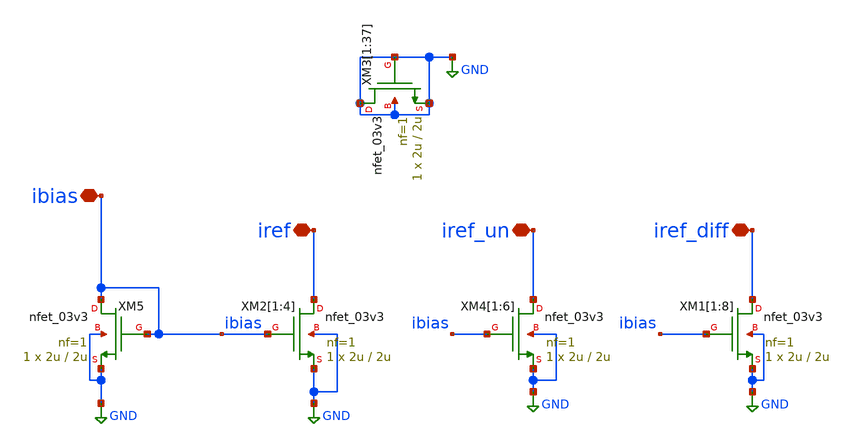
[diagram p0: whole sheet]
** sch_path: Voltage_Reference/LDO/CM_block.sch
**.subckt CM_block ibias iref iref_un iref_diff
*.iopin ibias
*.iopin iref
*.iopin iref_un
*.iopin iref_diff
XM4[1] iref_un ibias GND GND nfet_03v3 L=2u W=2u nf=1 ad='int((nf+1)/2) * W/nf * 0.18u' as='int((nf+2)/2) * W/nf * 0.18u'
+ pd='2*int((nf+1)/2) * (W/nf + 0.18u)' ps='2*int((nf+2)/2) * (W/nf + 0.18u)' nrd='0.18u / W' nrs='0.18u / W'
+ sa=0 sb=0 sd=0 m=1
XM4[2] iref_un ibias GND GND nfet_03v3 L=2u W=2u nf=1 ad='int((nf+1)/2) * W/nf * 0.18u' as='int((nf+2)/2) * W/nf * 0.18u'
+ pd='2*int((nf+1)/2) * (W/nf + 0.18u)' ps='2*int((nf+2)/2) * (W/nf + 0.18u)' nrd='0.18u / W' nrs='0.18u / W'
+ sa=0 sb=0 sd=0 m=1
XM4[3] iref_un ibias GND GND nfet_03v3 L=2u W=2u nf=1 ad='int((nf+1)/2) * W/nf * 0.18u' as='int((nf+2)/2) * W/nf * 0.18u'
+ pd='2*int((nf+1)/2) * (W/nf + 0.18u)' ps='2*int((nf+2)/2) * (W/nf + 0.18u)' nrd='0.18u / W' nrs='0.18u / W'
+ sa=0 sb=0 sd=0 m=1
XM4[4] iref_un ibias GND GND nfet_03v3 L=2u W=2u nf=1 ad='int((nf+1)/2) * W/nf * 0.18u' as='int((nf+2)/2) * W/nf * 0.18u'
+ pd='2*int((nf+1)/2) * (W/nf + 0.18u)' ps='2*int((nf+2)/2) * (W/nf + 0.18u)' nrd='0.18u / W' nrs='0.18u / W'
+ sa=0 sb=0 sd=0 m=1
XM4[5] iref_un ibias GND GND nfet_03v3 L=2u W=2u nf=1 ad='int((nf+1)/2) * W/nf * 0.18u' as='int((nf+2)/2) * W/nf * 0.18u'
+ pd='2*int((nf+1)/2) * (W/nf + 0.18u)' ps='2*int((nf+2)/2) * (W/nf + 0.18u)' nrd='0.18u / W' nrs='0.18u / W'
+ sa=0 sb=0 sd=0 m=1
XM4[6] iref_un ibias GND GND nfet_03v3 L=2u W=2u nf=1 ad='int((nf+1)/2) * W/nf * 0.18u' as='int((nf+2)/2) * W/nf * 0.18u'
+ pd='2*int((nf+1)/2) * (W/nf + 0.18u)' ps='2*int((nf+2)/2) * (W/nf + 0.18u)' nrd='0.18u / W' nrs='0.18u / W'
+ sa=0 sb=0 sd=0 m=1
XM1[1] iref_diff ibias GND GND nfet_03v3 L=2u W=2u nf=1 ad='int((nf+1)/2) * W/nf * 0.18u' as='int((nf+2)/2) * W/nf * 0.18u'
+ pd='2*int((nf+1)/2) * (W/nf + 0.18u)' ps='2*int((nf+2)/2) * (W/nf + 0.18u)' nrd='0.18u / W' nrs='0.18u / W'
+ sa=0 sb=0 sd=0 m=1
XM1[2] iref_diff ibias GND GND nfet_03v3 L=2u W=2u nf=1 ad='int((nf+1)/2) * W/nf * 0.18u' as='int((nf+2)/2) * W/nf * 0.18u'
+ pd='2*int((nf+1)/2) * (W/nf + 0.18u)' ps='2*int((nf+2)/2) * (W/nf + 0.18u)' nrd='0.18u / W' nrs='0.18u / W'
+ sa=0 sb=0 sd=0 m=1
XM1[3] iref_diff ibias GND GND nfet_03v3 L=2u W=2u nf=1 ad='int((nf+1)/2) * W/nf * 0.18u' as='int((nf+2)/2) * W/nf * 0.18u'
+ pd='2*int((nf+1)/2) * (W/nf + 0.18u)' ps='2*int((nf+2)/2) * (W/nf + 0.18u)' nrd='0.18u / W' nrs='0.18u / W'
+ sa=0 sb=0 sd=0 m=1
XM1[4] iref_diff ibias GND GND nfet_03v3 L=2u W=2u nf=1 ad='int((nf+1)/2) * W/nf * 0.18u' as='int((nf+2)/2) * W/nf * 0.18u'
+ pd='2*int((nf+1)/2) * (W/nf + 0.18u)' ps='2*int((nf+2)/2) * (W/nf + 0.18u)' nrd='0.18u / W' nrs='0.18u / W'
+ sa=0 sb=0 sd=0 m=1
XM1[5] iref_diff ibias GND GND nfet_03v3 L=2u W=2u nf=1 ad='int((nf+1)/2) * W/nf * 0.18u' as='int((nf+2)/2) * W/nf * 0.18u'
+ pd='2*int((nf+1)/2) * (W/nf + 0.18u)' ps='2*int((nf+2)/2) * (W/nf + 0.18u)' nrd='0.18u / W' nrs='0.18u / W'
+ sa=0 sb=0 sd=0 m=1
XM1[6] iref_diff ibias GND GND nfet_03v3 L=2u W=2u nf=1 ad='int((nf+1)/2) * W/nf * 0.18u' as='int((nf+2)/2) * W/nf * 0.18u'
+ pd='2*int((nf+1)/2) * (W/nf + 0.18u)' ps='2*int((nf+2)/2) * (W/nf + 0.18u)' nrd='0.18u / W' nrs='0.18u / W'
+ sa=0 sb=0 sd=0 m=1
XM1[7] iref_diff ibias GND GND nfet_03v3 L=2u W=2u nf=1 ad='int((nf+1)/2) * W/nf * 0.18u' as='int((nf+2)/2) * W/nf * 0.18u'
+ pd='2*int((nf+1)/2) * (W/nf + 0.18u)' ps='2*int((nf+2)/2) * (W/nf + 0.18u)' nrd='0.18u / W' nrs='0.18u / W'
+ sa=0 sb=0 sd=0 m=1
XM1[8] iref_diff ibias GND GND nfet_03v3 L=2u W=2u nf=1 ad='int((nf+1)/2) * W/nf * 0.18u' as='int((nf+2)/2) * W/nf * 0.18u'
+ pd='2*int((nf+1)/2) * (W/nf + 0.18u)' ps='2*int((nf+2)/2) * (W/nf + 0.18u)' nrd='0.18u / W' nrs='0.18u / W'
+ sa=0 sb=0 sd=0 m=1
XM2[1] iref ibias GND GND nfet_03v3 L=2u W=2u nf=1 ad='int((nf+1)/2) * W/nf * 0.18u' as='int((nf+2)/2) * W/nf * 0.18u'
+ pd='2*int((nf+1)/2) * (W/nf + 0.18u)' ps='2*int((nf+2)/2) * (W/nf + 0.18u)' nrd='0.18u / W' nrs='0.18u / W'
+ sa=0 sb=0 sd=0 m=1
XM2[2] iref ibias GND GND nfet_03v3 L=2u W=2u nf=1 ad='int((nf+1)/2) * W/nf * 0.18u' as='int((nf+2)/2) * W/nf * 0.18u'
+ pd='2*int((nf+1)/2) * (W/nf + 0.18u)' ps='2*int((nf+2)/2) * (W/nf + 0.18u)' nrd='0.18u / W' nrs='0.18u / W'
+ sa=0 sb=0 sd=0 m=1
XM2[3] iref ibias GND GND nfet_03v3 L=2u W=2u nf=1 ad='int((nf+1)/2) * W/nf * 0.18u' as='int((nf+2)/2) * W/nf * 0.18u'
+ pd='2*int((nf+1)/2) * (W/nf + 0.18u)' ps='2*int((nf+2)/2) * (W/nf + 0.18u)' nrd='0.18u / W' nrs='0.18u / W'
+ sa=0 sb=0 sd=0 m=1
XM2[4] iref ibias GND GND nfet_03v3 L=2u W=2u nf=1 ad='int((nf+1)/2) * W/nf * 0.18u' as='int((nf+2)/2) * W/nf * 0.18u'
+ pd='2*int((nf+1)/2) * (W/nf + 0.18u)' ps='2*int((nf+2)/2) * (W/nf + 0.18u)' nrd='0.18u / W' nrs='0.18u / W'
+ sa=0 sb=0 sd=0 m=1
XM5 ibias ibias GND GND nfet_03v3 L=2u W=2u nf=1 ad='int((nf+1)/2) * W/nf * 0.18u' as='int((nf+2)/2) * W/nf * 0.18u'
+ pd='2*int((nf+1)/2) * (W/nf + 0.18u)' ps='2*int((nf+2)/2) * (W/nf + 0.18u)' nrd='0.18u / W' nrs='0.18u / W'
+ sa=0 sb=0 sd=0 m=1
XM3[1] GND GND GND GND nfet_03v3 L=2u W=2u nf=1 ad='int((nf+1)/2) * W/nf * 0.18u' as='int((nf+2)/2) * W/nf * 0.18u'
+ pd='2*int((nf+1)/2) * (W/nf + 0.18u)' ps='2*int((nf+2)/2) * (W/nf + 0.18u)' nrd='0.18u / W' nrs='0.18u / W'
+ sa=0 sb=0 sd=0 m=1
XM3[2] GND GND GND GND nfet_03v3 L=2u W=2u nf=1 ad='int((nf+1)/2) * W/nf * 0.18u' as='int((nf+2)/2) * W/nf * 0.18u'
+ pd='2*int((nf+1)/2) * (W/nf + 0.18u)' ps='2*int((nf+2)/2) * (W/nf + 0.18u)' nrd='0.18u / W' nrs='0.18u / W'
+ sa=0 sb=0 sd=0 m=1
XM3[3] GND GND GND GND nfet_03v3 L=2u W=2u nf=1 ad='int((nf+1)/2) * W/nf * 0.18u' as='int((nf+2)/2) * W/nf * 0.18u'
+ pd='2*int((nf+1)/2) * (W/nf + 0.18u)' ps='2*int((nf+2)/2) * (W/nf + 0.18u)' nrd='0.18u / W' nrs='0.18u / W'
+ sa=0 sb=0 sd=0 m=1
XM3[4] GND GND GND GND nfet_03v3 L=2u W=2u nf=1 ad='int((nf+1)/2) * W/nf * 0.18u' as='int((nf+2)/2) * W/nf * 0.18u'
+ pd='2*int((nf+1)/2) * (W/nf + 0.18u)' ps='2*int((nf+2)/2) * (W/nf + 0.18u)' nrd='0.18u / W' nrs='0.18u / W'
+ sa=0 sb=0 sd=0 m=1
XM3[5] GND GND GND GND nfet_03v3 L=2u W=2u nf=1 ad='int((nf+1)/2) * W/nf * 0.18u' as='int((nf+2)/2) * W/nf * 0.18u'
+ pd='2*int((nf+1)/2) * (W/nf + 0.18u)' ps='2*int((nf+2)/2) * (W/nf + 0.18u)' nrd='0.18u / W' nrs='0.18u / W'
+ sa=0 sb=0 sd=0 m=1
XM3[6] GND GND GND GND nfet_03v3 L=2u W=2u nf=1 ad='int((nf+1)/2) * W/nf * 0.18u' as='int((nf+2)/2) * W/nf * 0.18u'
+ pd='2*int((nf+1)/2) * (W/nf + 0.18u)' ps='2*int((nf+2)/2) * (W/nf + 0.18u)' nrd='0.18u / W' nrs='0.18u / W'
+ sa=0 sb=0 sd=0 m=1
XM3[7] GND GND GND GND nfet_03v3 L=2u W=2u nf=1 ad='int((nf+1)/2) * W/nf * 0.18u' as='int((nf+2)/2) * W/nf * 0.18u'
+ pd='2*int((nf+1)/2) * (W/nf + 0.18u)' ps='2*int((nf+2)/2) * (W/nf + 0.18u)' nrd='0.18u / W' nrs='0.18u / W'
+ sa=0 sb=0 sd=0 m=1
XM3[8] GND GND GND GND nfet_03v3 L=2u W=2u nf=1 ad='int((nf+1)/2) * W/nf * 0.18u' as='int((nf+2)/2) * W/nf * 0.18u'
+ pd='2*int((nf+1)/2) * (W/nf + 0.18u)' ps='2*int((nf+2)/2) * (W/nf + 0.18u)' nrd='0.18u / W' nrs='0.18u / W'
+ sa=0 sb=0 sd=0 m=1
XM3[9] GND GND GND GND nfet_03v3 L=2u W=2u nf=1 ad='int((nf+1)/2) * W/nf * 0.18u' as='int((nf+2)/2) * W/nf * 0.18u'
+ pd='2*int((nf+1)/2) * (W/nf + 0.18u)' ps='2*int((nf+2)/2) * (W/nf + 0.18u)' nrd='0.18u / W' nrs='0.18u / W'
+ sa=0 sb=0 sd=0 m=1
XM3[10] GND GND GND GND nfet_03v3 L=2u W=2u nf=1 ad='int((nf+1)/2) * W/nf * 0.18u' as='int((nf+2)/2) * W/nf * 0.18u'
+ pd='2*int((nf+1)/2) * (W/nf + 0.18u)' ps='2*int((nf+2)/2) * (W/nf + 0.18u)' nrd='0.18u / W' nrs='0.18u / W'
+ sa=0 sb=0 sd=0 m=1
XM3[11] GND GND GND GND nfet_03v3 L=2u W=2u nf=1 ad='int((nf+1)/2) * W/nf * 0.18u' as='int((nf+2)/2) * W/nf * 0.18u'
+ pd='2*int((nf+1)/2) * (W/nf + 0.18u)' ps='2*int((nf+2)/2) * (W/nf + 0.18u)' nrd='0.18u / W' nrs='0.18u / W'
+ sa=0 sb=0 sd=0 m=1
XM3[12] GND GND GND GND nfet_03v3 L=2u W=2u nf=1 ad='int((nf+1)/2) * W/nf * 0.18u' as='int((nf+2)/2) * W/nf * 0.18u'
+ pd='2*int((nf+1)/2) * (W/nf + 0.18u)' ps='2*int((nf+2)/2) * (W/nf + 0.18u)' nrd='0.18u / W' nrs='0.18u / W'
+ sa=0 sb=0 sd=0 m=1
XM3[13] GND GND GND GND nfet_03v3 L=2u W=2u nf=1 ad='int((nf+1)/2) * W/nf * 0.18u' as='int((nf+2)/2) * W/nf * 0.18u'
+ pd='2*int((nf+1)/2) * (W/nf + 0.18u)' ps='2*int((nf+2)/2) * (W/nf + 0.18u)' nrd='0.18u / W' nrs='0.18u / W'
+ sa=0 sb=0 sd=0 m=1
XM3[14] GND GND GND GND nfet_03v3 L=2u W=2u nf=1 ad='int((nf+1)/2) * W/nf * 0.18u' as='int((nf+2)/2) * W/nf * 0.18u'
+ pd='2*int((nf+1)/2) * (W/nf + 0.18u)' ps='2*int((nf+2)/2) * (W/nf + 0.18u)' nrd='0.18u / W' nrs='0.18u / W'
+ sa=0 sb=0 sd=0 m=1
XM3[15] GND GND GND GND nfet_03v3 L=2u W=2u nf=1 ad='int((nf+1)/2) * W/nf * 0.18u' as='int((nf+2)/2) * W/nf * 0.18u'
+ pd='2*int((nf+1)/2) * (W/nf + 0.18u)' ps='2*int((nf+2)/2) * (W/nf + 0.18u)' nrd='0.18u / W' nrs='0.18u / W'
+ sa=0 sb=0 sd=0 m=1
XM3[16] GND GND GND GND nfet_03v3 L=2u W=2u nf=1 ad='int((nf+1)/2) * W/nf * 0.18u' as='int((nf+2)/2) * W/nf * 0.18u'
+ pd='2*int((nf+1)/2) * (W/nf + 0.18u)' ps='2*int((nf+2)/2) * (W/nf + 0.18u)' nrd='0.18u / W' nrs='0.18u / W'
+ sa=0 sb=0 sd=0 m=1
XM3[17] GND GND GND GND nfet_03v3 L=2u W=2u nf=1 ad='int((nf+1)/2) * W/nf * 0.18u' as='int((nf+2)/2) * W/nf * 0.18u'
+ pd='2*int((nf+1)/2) * (W/nf + 0.18u)' ps='2*int((nf+2)/2) * (W/nf + 0.18u)' nrd='0.18u / W' nrs='0.18u / W'
+ sa=0 sb=0 sd=0 m=1
XM3[18] GND GND GND GND nfet_03v3 L=2u W=2u nf=1 ad='int((nf+1)/2) * W/nf * 0.18u' as='int((nf+2)/2) * W/nf * 0.18u'
+ pd='2*int((nf+1)/2) * (W/nf + 0.18u)' ps='2*int((nf+2)/2) * (W/nf + 0.18u)' nrd='0.18u / W' nrs='0.18u / W'
+ sa=0 sb=0 sd=0 m=1
XM3[19] GND GND GND GND nfet_03v3 L=2u W=2u nf=1 ad='int((nf+1)/2) * W/nf * 0.18u' as='int((nf+2)/2) * W/nf * 0.18u'
+ pd='2*int((nf+1)/2) * (W/nf + 0.18u)' ps='2*int((nf+2)/2) * (W/nf + 0.18u)' nrd='0.18u / W' nrs='0.18u / W'
+ sa=0 sb=0 sd=0 m=1
XM3[20] GND GND GND GND nfet_03v3 L=2u W=2u nf=1 ad='int((nf+1)/2) * W/nf * 0.18u' as='int((nf+2)/2) * W/nf * 0.18u'
+ pd='2*int((nf+1)/2) * (W/nf + 0.18u)' ps='2*int((nf+2)/2) * (W/nf + 0.18u)' nrd='0.18u / W' nrs='0.18u / W'
+ sa=0 sb=0 sd=0 m=1
XM3[21] GND GND GND GND nfet_03v3 L=2u W=2u nf=1 ad='int((nf+1)/2) * W/nf * 0.18u' as='int((nf+2)/2) * W/nf * 0.18u'
+ pd='2*int((nf+1)/2) * (W/nf + 0.18u)' ps='2*int((nf+2)/2) * (W/nf + 0.18u)' nrd='0.18u / W' nrs='0.18u / W'
+ sa=0 sb=0 sd=0 m=1
XM3[22] GND GND GND GND nfet_03v3 L=2u W=2u nf=1 ad='int((nf+1)/2) * W/nf * 0.18u' as='int((nf+2)/2) * W/nf * 0.18u'
+ pd='2*int((nf+1)/2) * (W/nf + 0.18u)' ps='2*int((nf+2)/2) * (W/nf + 0.18u)' nrd='0.18u / W' nrs='0.18u / W'
+ sa=0 sb=0 sd=0 m=1
XM3[23] GND GND GND GND nfet_03v3 L=2u W=2u nf=1 ad='int((nf+1)/2) * W/nf * 0.18u' as='int((nf+2)/2) * W/nf * 0.18u'
+ pd='2*int((nf+1)/2) * (W/nf + 0.18u)' ps='2*int((nf+2)/2) * (W/nf + 0.18u)' nrd='0.18u / W' nrs='0.18u / W'
+ sa=0 sb=0 sd=0 m=1
XM3[24] GND GND GND GND nfet_03v3 L=2u W=2u nf=1 ad='int((nf+1)/2) * W/nf * 0.18u' as='int((nf+2)/2) * W/nf * 0.18u'
+ pd='2*int((nf+1)/2) * (W/nf + 0.18u)' ps='2*int((nf+2)/2) * (W/nf + 0.18u)' nrd='0.18u / W' nrs='0.18u / W'
+ sa=0 sb=0 sd=0 m=1
XM3[25] GND GND GND GND nfet_03v3 L=2u W=2u nf=1 ad='int((nf+1)/2) * W/nf * 0.18u' as='int((nf+2)/2) * W/nf * 0.18u'
+ pd='2*int((nf+1)/2) * (W/nf + 0.18u)' ps='2*int((nf+2)/2) * (W/nf + 0.18u)' nrd='0.18u / W' nrs='0.18u / W'
+ sa=0 sb=0 sd=0 m=1
XM3[26] GND GND GND GND nfet_03v3 L=2u W=2u nf=1 ad='int((nf+1)/2) * W/nf * 0.18u' as='int((nf+2)/2) * W/nf * 0.18u'
+ pd='2*int((nf+1)/2) * (W/nf + 0.18u)' ps='2*int((nf+2)/2) * (W/nf + 0.18u)' nrd='0.18u / W' nrs='0.18u / W'
+ sa=0 sb=0 sd=0 m=1
XM3[27] GND GND GND GND nfet_03v3 L=2u W=2u nf=1 ad='int((nf+1)/2) * W/nf * 0.18u' as='int((nf+2)/2) * W/nf * 0.18u'
+ pd='2*int((nf+1)/2) * (W/nf + 0.18u)' ps='2*int((nf+2)/2) * (W/nf + 0.18u)' nrd='0.18u / W' nrs='0.18u / W'
+ sa=0 sb=0 sd=0 m=1
XM3[28] GND GND GND GND nfet_03v3 L=2u W=2u nf=1 ad='int((nf+1)/2) * W/nf * 0.18u' as='int((nf+2)/2) * W/nf * 0.18u'
+ pd='2*int((nf+1)/2) * (W/nf + 0.18u)' ps='2*int((nf+2)/2) * (W/nf + 0.18u)' nrd='0.18u / W' nrs='0.18u / W'
+ sa=0 sb=0 sd=0 m=1
XM3[29] GND GND GND GND nfet_03v3 L=2u W=2u nf=1 ad='int((nf+1)/2) * W/nf * 0.18u' as='int((nf+2)/2) * W/nf * 0.18u'
+ pd='2*int((nf+1)/2) * (W/nf + 0.18u)' ps='2*int((nf+2)/2) * (W/nf + 0.18u)' nrd='0.18u / W' nrs='0.18u / W'
+ sa=0 sb=0 sd=0 m=1
XM3[30] GND GND GND GND nfet_03v3 L=2u W=2u nf=1 ad='int((nf+1)/2) * W/nf * 0.18u' as='int((nf+2)/2) * W/nf * 0.18u'
+ pd='2*int((nf+1)/2) * (W/nf + 0.18u)' ps='2*int((nf+2)/2) * (W/nf + 0.18u)' nrd='0.18u / W' nrs='0.18u / W'
+ sa=0 sb=0 sd=0 m=1
XM3[31] GND GND GND GND nfet_03v3 L=2u W=2u nf=1 ad='int((nf+1)/2) * W/nf * 0.18u' as='int((nf+2)/2) * W/nf * 0.18u'
+ pd='2*int((nf+1)/2) * (W/nf + 0.18u)' ps='2*int((nf+2)/2) * (W/nf + 0.18u)' nrd='0.18u / W' nrs='0.18u / W'
+ sa=0 sb=0 sd=0 m=1
XM3[32] GND GND GND GND nfet_03v3 L=2u W=2u nf=1 ad='int((nf+1)/2) * W/nf * 0.18u' as='int((nf+2)/2) * W/nf * 0.18u'
+ pd='2*int((nf+1)/2) * (W/nf + 0.18u)' ps='2*int((nf+2)/2) * (W/nf + 0.18u)' nrd='0.18u / W' nrs='0.18u / W'
+ sa=0 sb=0 sd=0 m=1
XM3[33] GND GND GND GND nfet_03v3 L=2u W=2u nf=1 ad='int((nf+1)/2) * W/nf * 0.18u' as='int((nf+2)/2) * W/nf * 0.18u'
+ pd='2*int((nf+1)/2) * (W/nf + 0.18u)' ps='2*int((nf+2)/2) * (W/nf + 0.18u)' nrd='0.18u / W' nrs='0.18u / W'
+ sa=0 sb=0 sd=0 m=1
XM3[34] GND GND GND GND nfet_03v3 L=2u W=2u nf=1 ad='int((nf+1)/2) * W/nf * 0.18u' as='int((nf+2)/2) * W/nf * 0.18u'
+ pd='2*int((nf+1)/2) * (W/nf + 0.18u)' ps='2*int((nf+2)/2) * (W/nf + 0.18u)' nrd='0.18u / W' nrs='0.18u / W'
+ sa=0 sb=0 sd=0 m=1
XM3[35] GND GND GND GND nfet_03v3 L=2u W=2u nf=1 ad='int((nf+1)/2) * W/nf * 0.18u' as='int((nf+2)/2) * W/nf * 0.18u'
+ pd='2*int((nf+1)/2) * (W/nf + 0.18u)' ps='2*int((nf+2)/2) * (W/nf + 0.18u)' nrd='0.18u / W' nrs='0.18u / W'
+ sa=0 sb=0 sd=0 m=1
XM3[36] GND GND GND GND nfet_03v3 L=2u W=2u nf=1 ad='int((nf+1)/2) * W/nf * 0.18u' as='int((nf+2)/2) * W/nf * 0.18u'
+ pd='2*int((nf+1)/2) * (W/nf + 0.18u)' ps='2*int((nf+2)/2) * (W/nf + 0.18u)' nrd='0.18u / W' nrs='0.18u / W'
+ sa=0 sb=0 sd=0 m=1
XM3[37] GND GND GND GND nfet_03v3 L=2u W=2u nf=1 ad='int((nf+1)/2) * W/nf * 0.18u' as='int((nf+2)/2) * W/nf * 0.18u'
+ pd='2*int((nf+1)/2) * (W/nf + 0.18u)' ps='2*int((nf+2)/2) * (W/nf + 0.18u)' nrd='0.18u / W' nrs='0.18u / W'
+ sa=0 sb=0 sd=0 m=1
**.ends
.GLOBAL GND
.end
